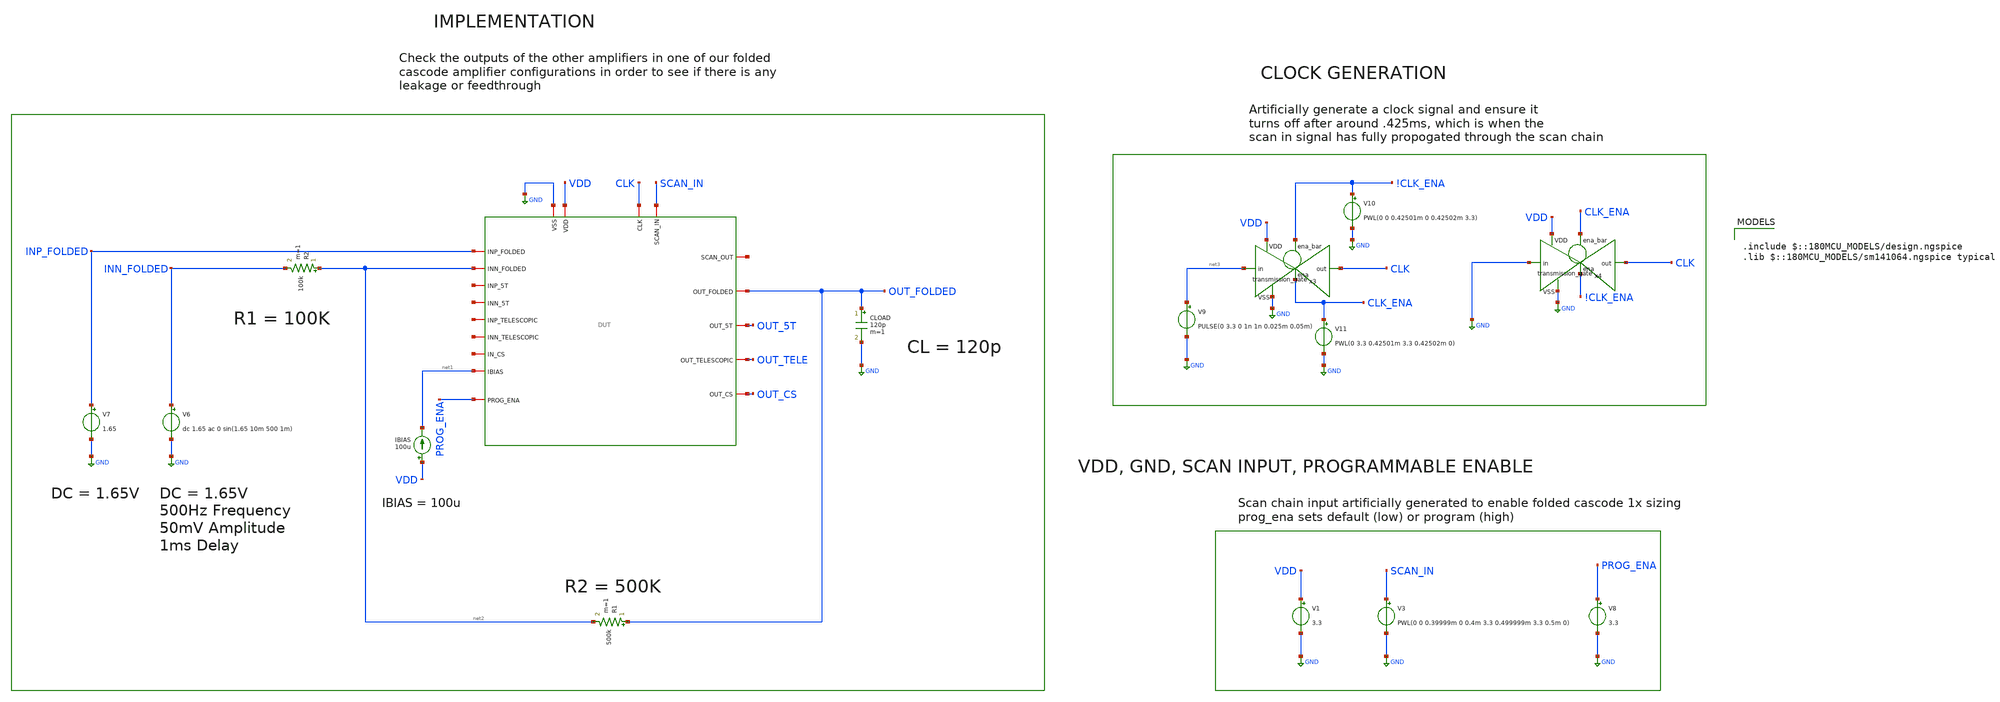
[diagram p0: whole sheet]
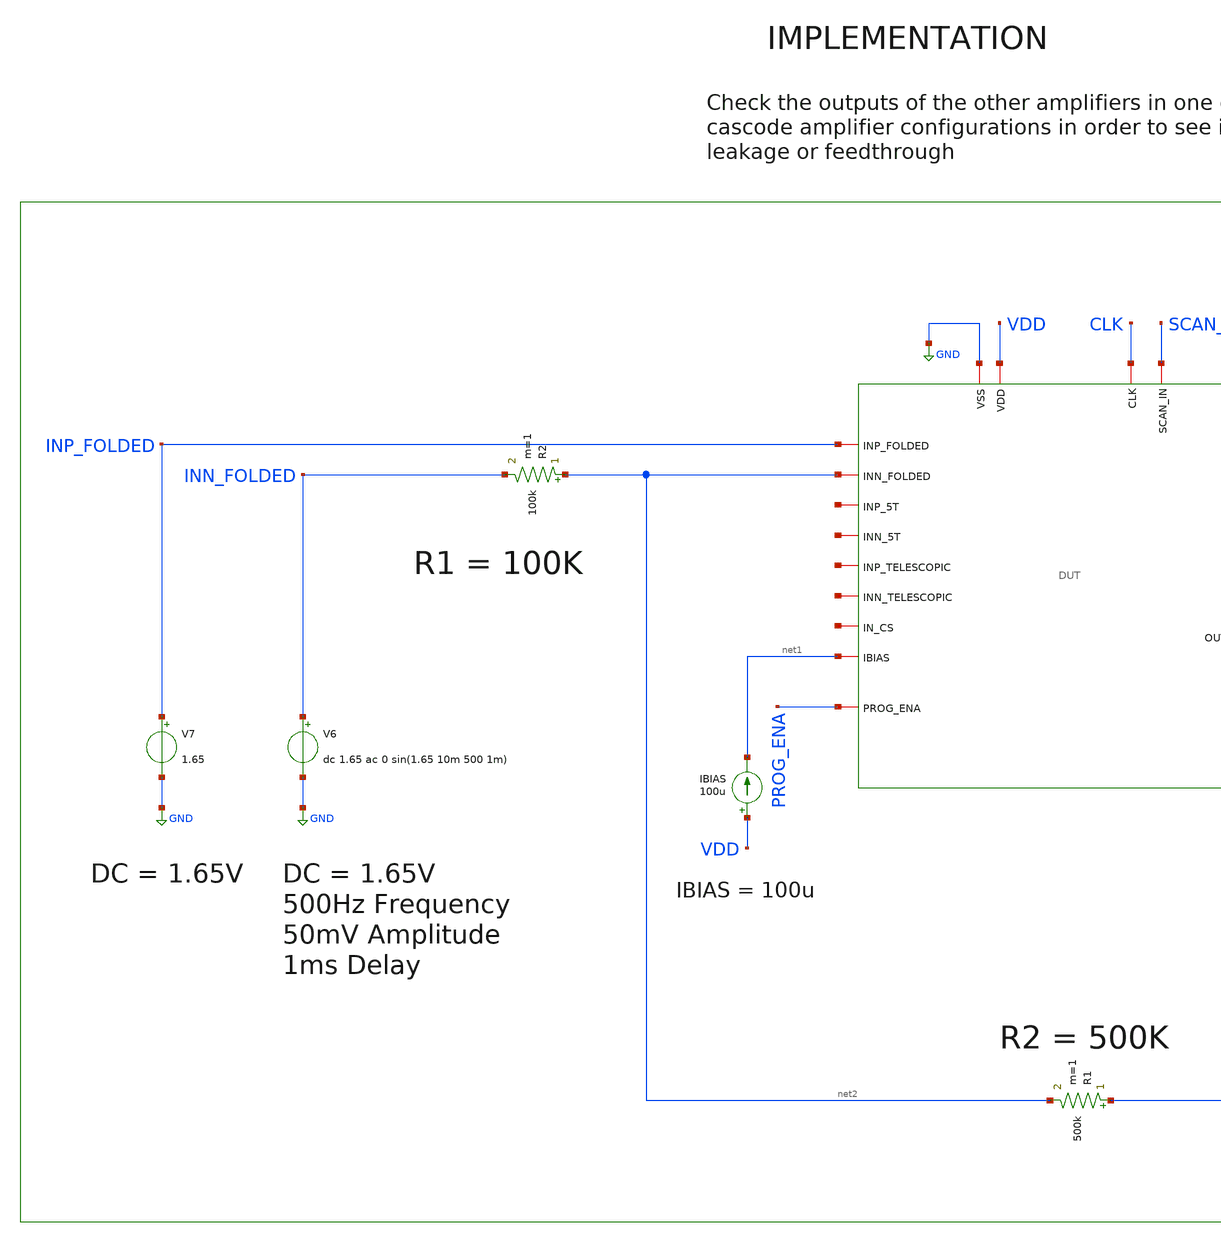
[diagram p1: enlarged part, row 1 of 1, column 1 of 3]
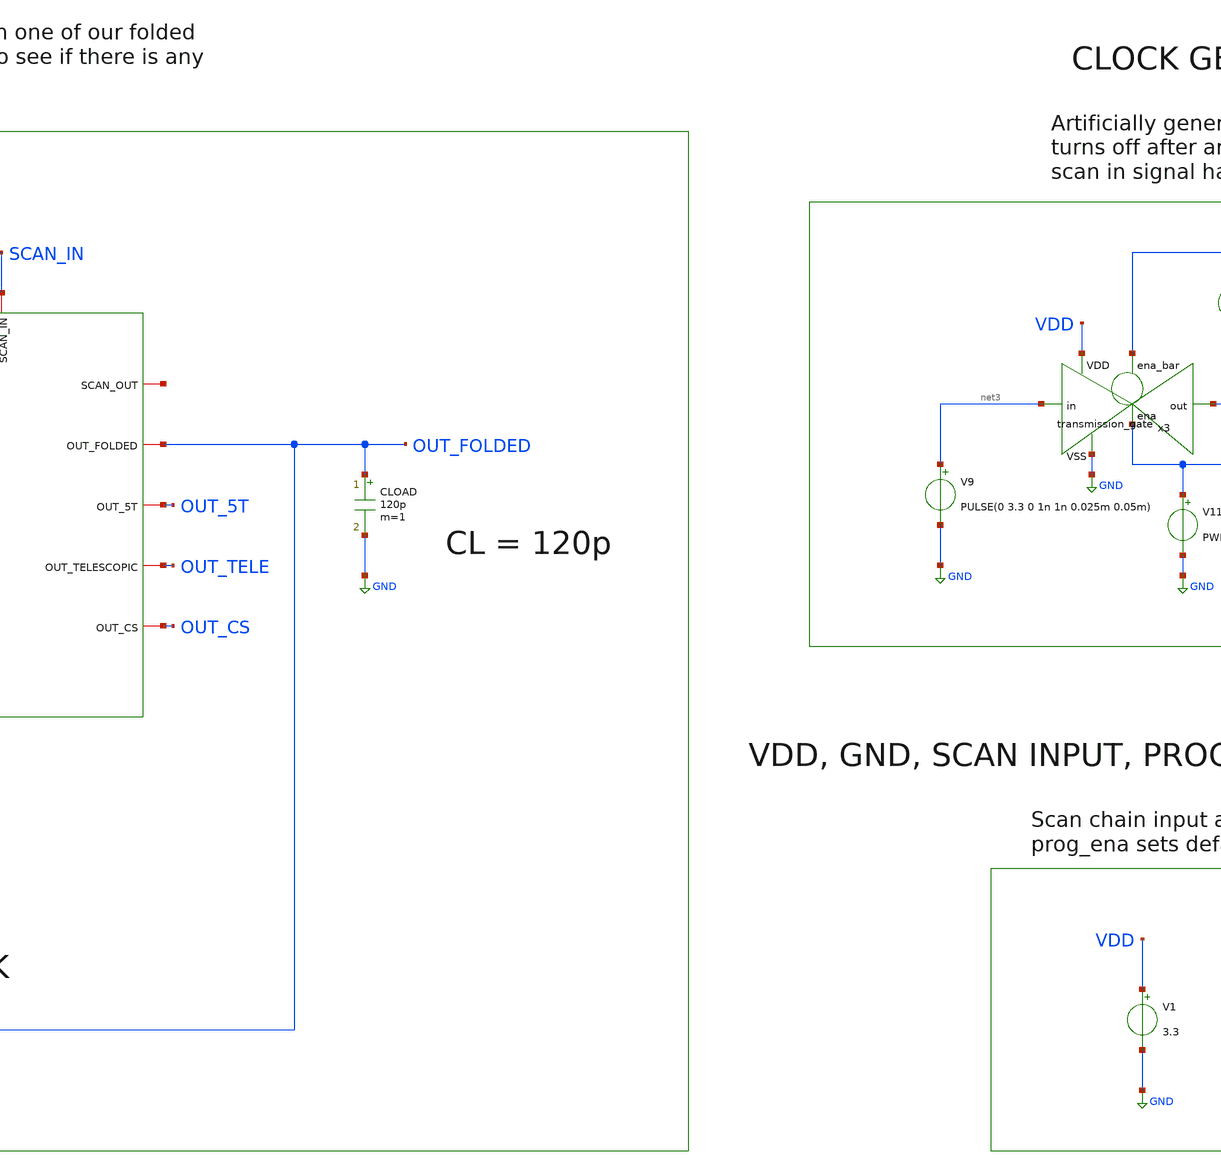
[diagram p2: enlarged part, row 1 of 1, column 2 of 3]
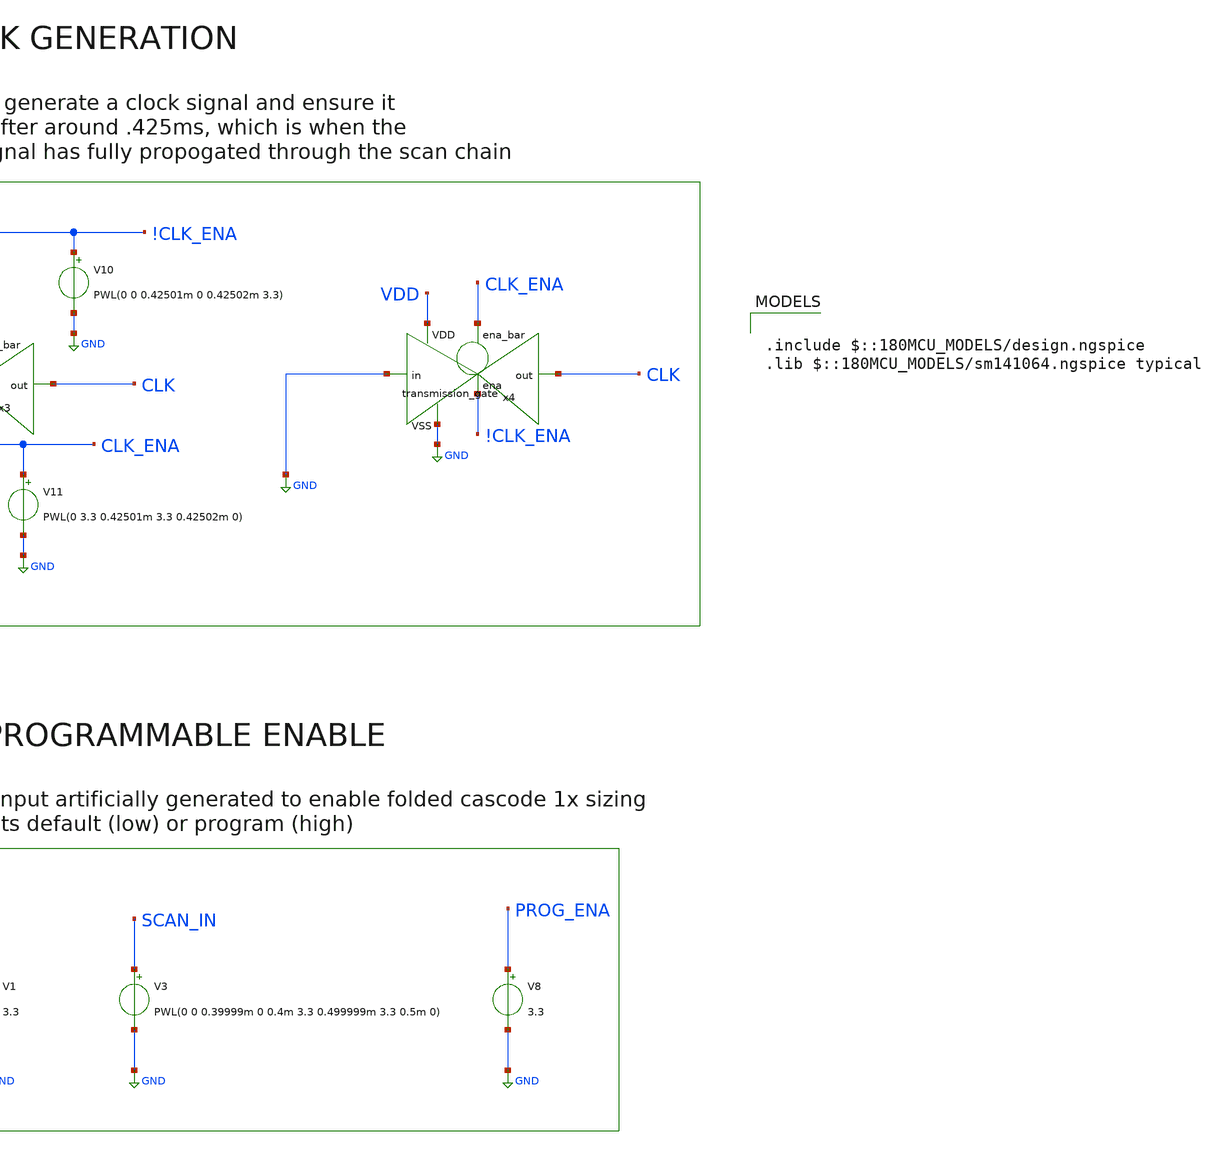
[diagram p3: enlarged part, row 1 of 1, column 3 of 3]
** sch_path: designs/libs/verification/ota_folded/output_isolation/output_isolation_tb.sch
**.subckt output_isolation_tb
V3 SCAN_IN GND PWL(0 0 0.39999m 0 0.4m 3.3 0.499999m 3.3 0.5m 0)
V1 VDD GND 3.3
IBIAS VDD net1 100u
V7 INP_FOLDED GND 1.65
CLOAD OUT_FOLDED GND 120p m=1
R2 net2 INN_FOLDED 100k m=1
V6 INN_FOLDED GND dc 1.65 ac 0 sin(1.65 10m 500 1m)
R1 OUT_FOLDED net2 500k m=1
x1 CLK net4 SCAN_IN GND VDD OUT_FOLDED INP_FOLDED OUT_5T net1 net2 net5 net6 net7 OUT_TELE OUT_CS
+ net8 net9 PROG_ENA DUT
V8 PROG_ENA GND 3.3
V9 net3 GND PULSE(0 3.3 0 1n 1n 0.025m 0.05m)
x3 !CLK_ENA VDD CLK net3 GND CLK_ENA transmission_gate
V10 !CLK_ENA GND PWL(0 0 0.42501m 0 0.42502m 3.3)
V11 CLK_ENA GND PWL(0 3.3 0.42501m 3.3 0.42502m 0)
x4 CLK_ENA VDD CLK GND GND !CLK_ENA transmission_gate
**** begin user architecture code

.include $::180MCU_MODELS/design.ngspice
.lib $::180MCU_MODELS/sm141064.ngspice typical



.control
tran 1u 5m

plot v(out_folded) v(out_5t) v(out_tele) v(out_cs)

meas tran folded_pp pp v(out_folded) from=2m to=5m
meas tran five_t_pp pp v(out_5t) from=2m to=5m
meas tran tele_pp pp v(out_tele) from=2m to=5m
meas tran cs_pp pp v(out_cs) from=2m to=5m

print folded_pp five_t_pp tele_pp cs_pp

let iso_5t = 20 * log(five_t_pp / folded_pp) / log(10)
let iso_tele = 20 * log(tele_pp / folded_pp) / log(10)
let iso_cs = 20 * log(cs_pp / folded_pp) / log(10)

print iso_5t iso_tele iso_cs
.endc


**** end user architecture code
**.ends
.GLOBAL GND
.end
